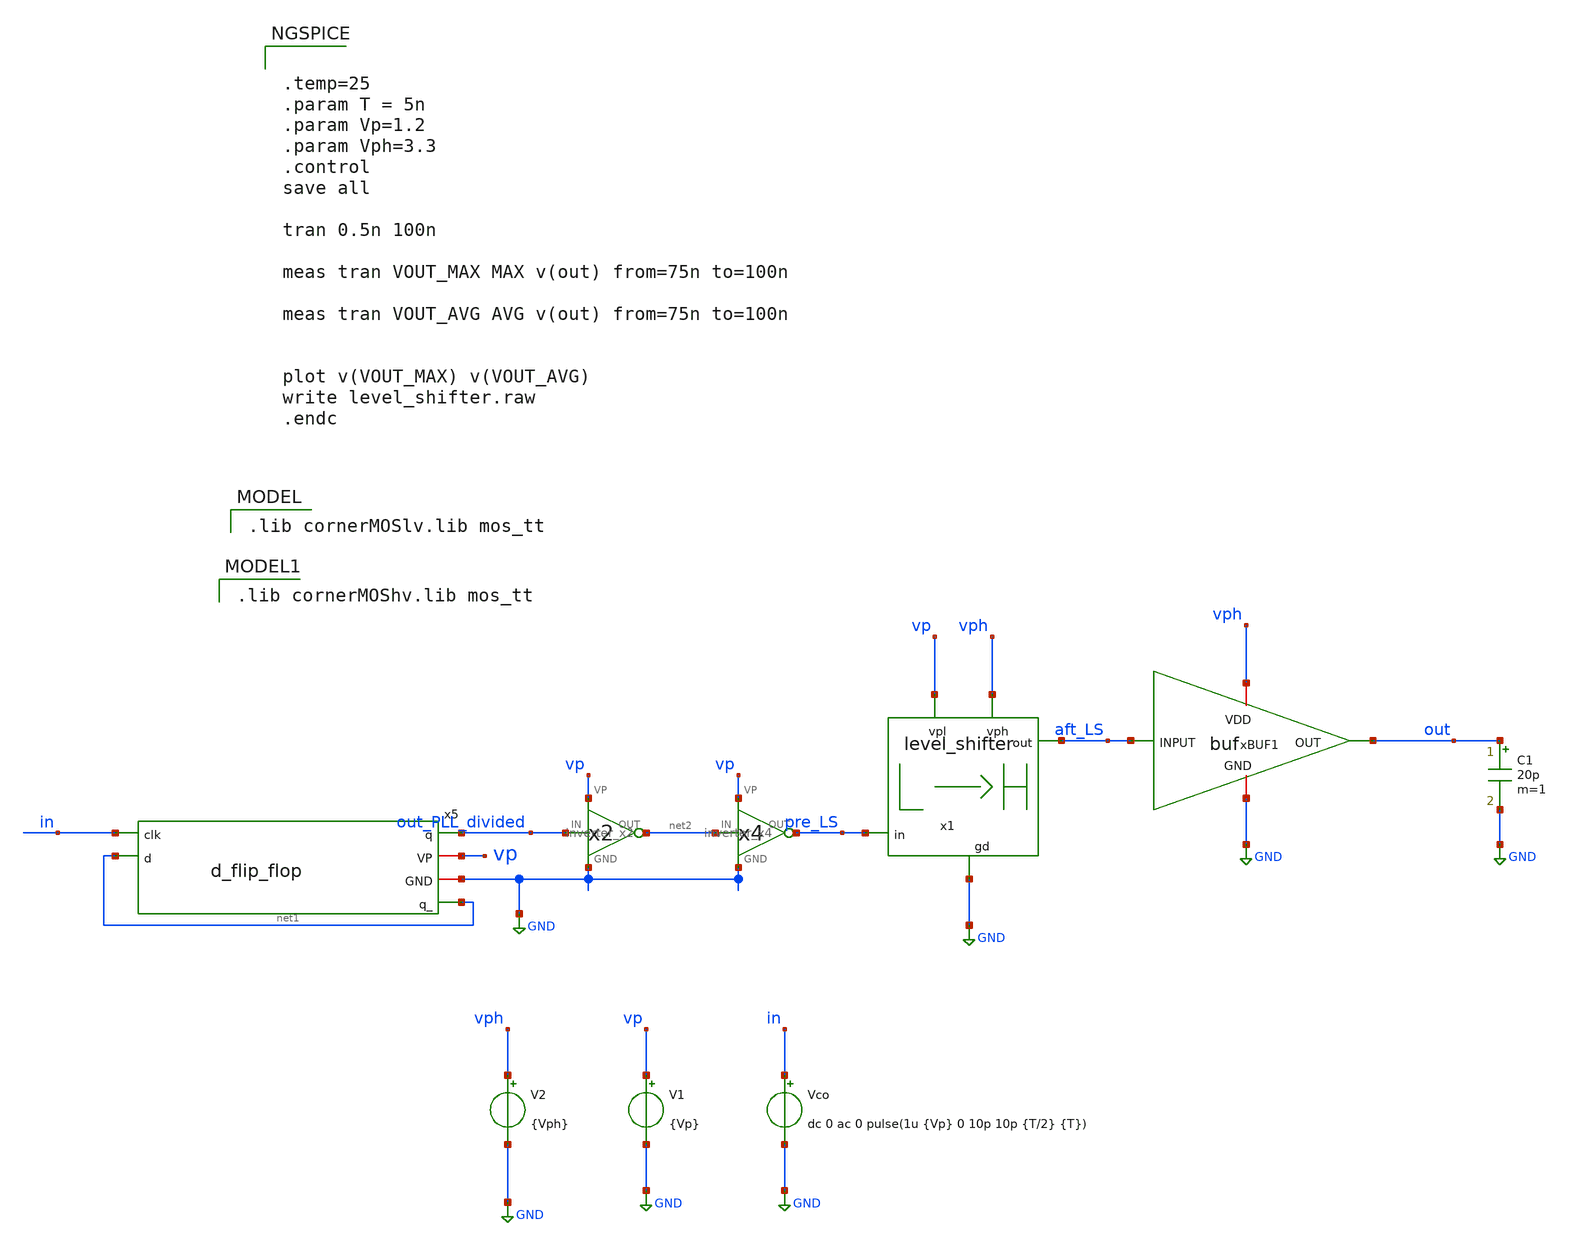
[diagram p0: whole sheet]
** sch_path: schematics/misc/level_shifter_tb.sch
**.subckt level_shifter_tb
x1 vph aft_LS vp pre_LS GND level_shifter
V1 vp GND {Vp}
V2 vph GND {Vph}
C1 out GND 20p m=1
Vco in GND dc 0 ac 0 pulse(1u {Vp} 0 10p 10p {T/2} {T})
x5 out_PLL_divided vp GND net1 in net1 d_flip_flop
x2 out_PLL_divided net2 vp GND inverter_x2
x3 net2 pre_LS vp GND inverter_x4
xBUF1 vph aft_LS out GND buf
**** begin user architecture code
 .lib cornerMOSlv.lib mos_tt



.temp=25
.param T = 5n
.param Vp=1.2
.param Vph=3.3
.control
save all

tran 0.5n 100n

meas tran VOUT_MAX MAX v(out) from=75n to=100n

meas tran VOUT_AVG AVG v(out) from=75n to=100n


plot v(VOUT_MAX) v(VOUT_AVG)
write level_shifter.raw
.endc


 .lib cornerMOShv.lib mos_tt

**** end user architecture code
**.ends
.GLOBAL GND
.end
